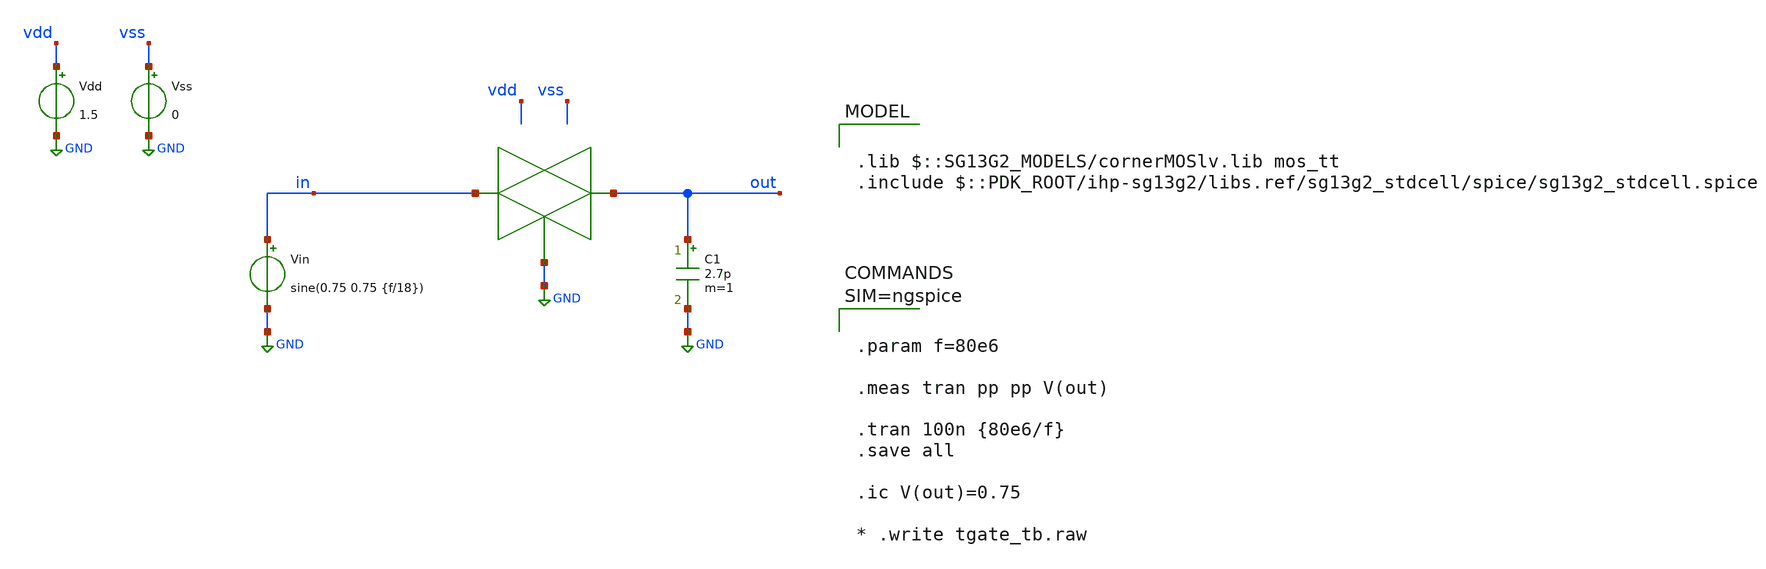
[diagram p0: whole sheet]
** sch_path: designs/tgate_bleed/tgate_tb.sch
**.subckt tgate_tb
Vdd vdd GND 1.5
Vss vss GND 0
C1 out GND 2.7p m=1
Vin in GND sine(0.75 0.75 {f/18})
**** begin user architecture code



.param f=80e6

.meas tran pp pp V(out)

.tran 100n {80e6/f}
.save all

.ic V(out)=0.75

* .write tgate_tb.raw




.lib $::SG13G2_MODELS/cornerMOSlv.lib mos_tt
.include $::PDK_ROOT/ihp-sg13g2/libs.ref/sg13g2_stdcell/spice/sg13g2_stdcell.spice

**** end user architecture code
**.ends
.GLOBAL GND
.end
